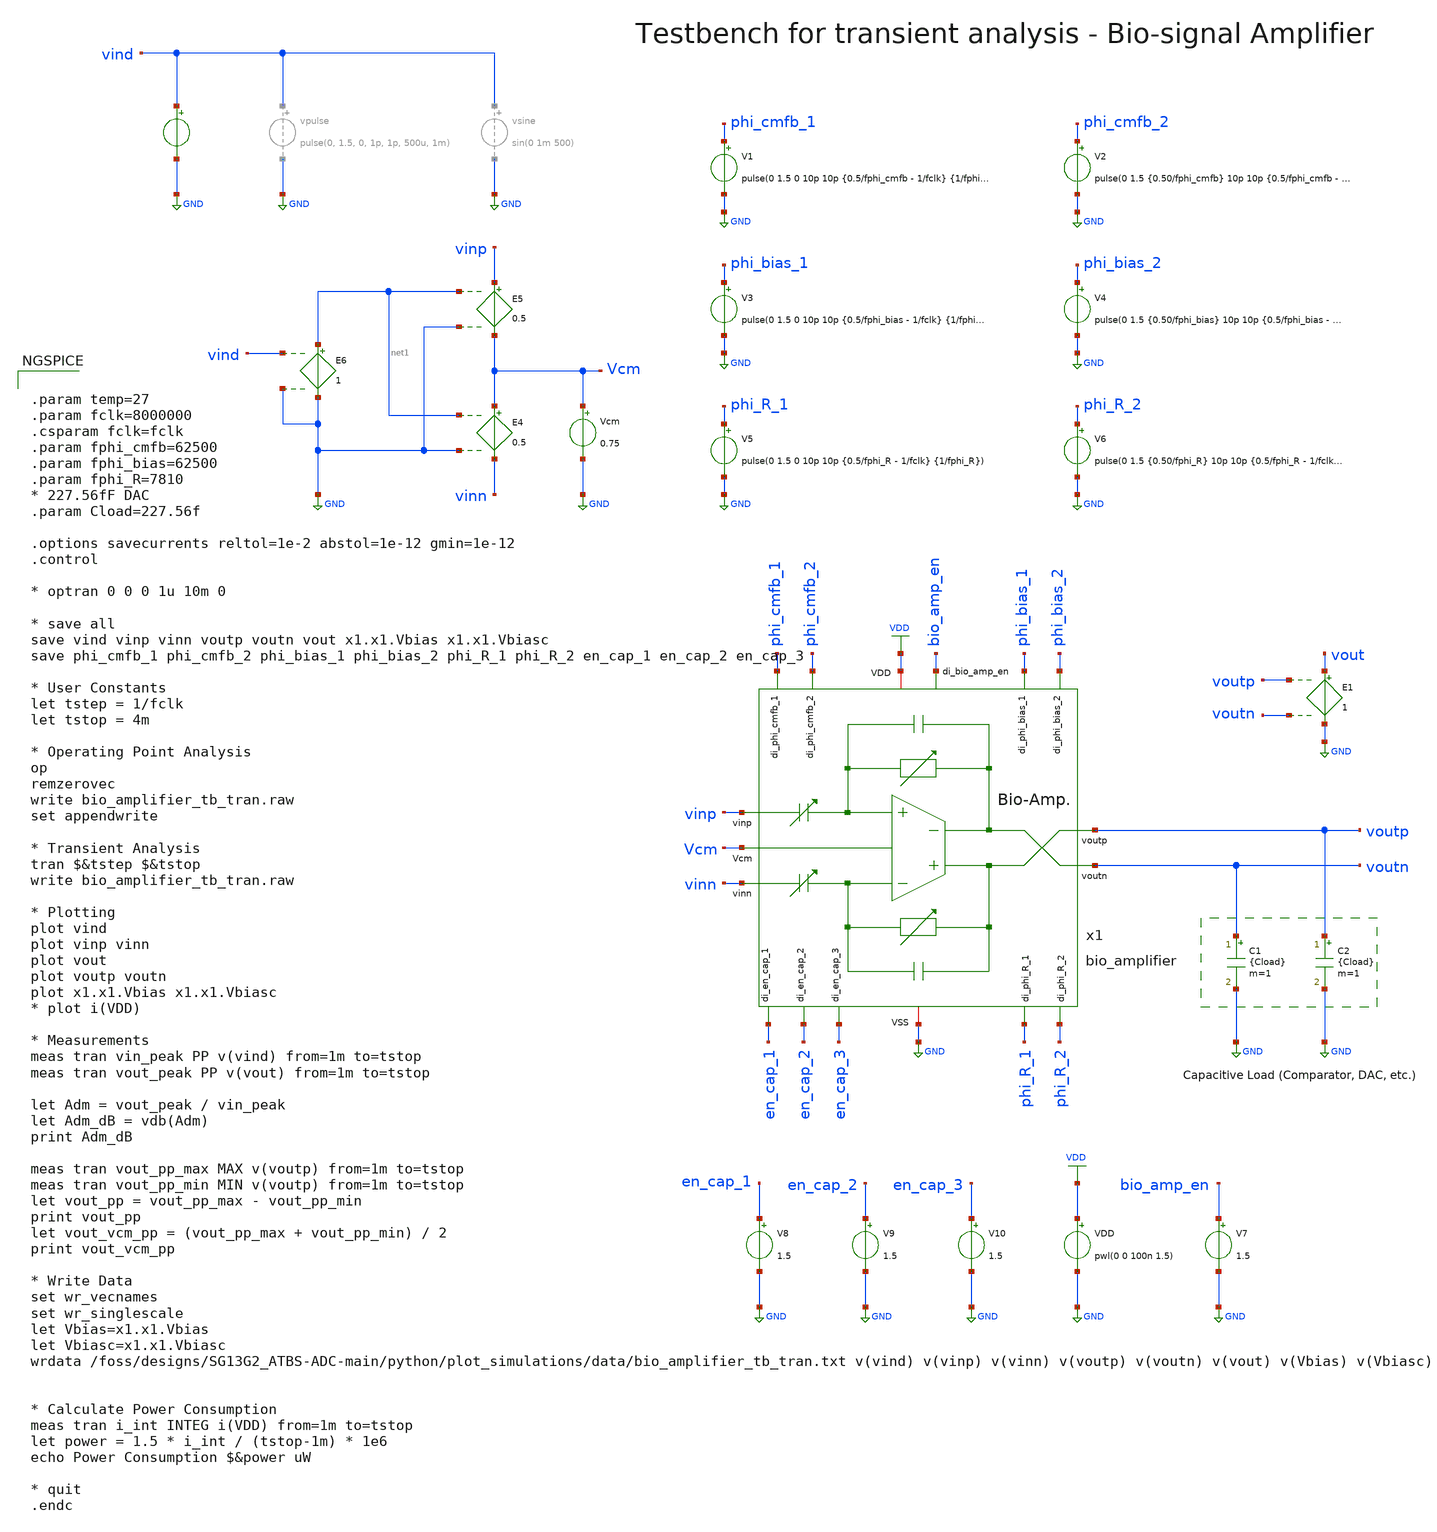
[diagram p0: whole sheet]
** sch_path: SG13G2_ATBS-ADC-main/xschem/bio_amplifier/testbenches/bio_amplifier_tb_tran.sch
**.subckt bio_amplifier_tb_tran
C1 voutn GND {Cload} m=1
x1 phi_bias_2 phi_bias_1 phi_R_2 phi_R_1 en_cap_3 en_cap_1 en_cap_2 phi_cmfb_2 phi_cmfb_1 voutp
+ bio_amp_en vinp Vcm voutn vinn VDD GND bio_amplifier
C2 voutp GND {Cload} m=1
V1 phi_cmfb_1 GND pulse(0 1.5 0 10p 10p {0.5/fphi_cmfb - 1/fclk} {1/fphi_cmfb})
Vcm Vcm GND 0.75
E4 Vcm vinn net1 GND 0.5
E5 vinp Vcm net1 GND 0.5
E6 net1 GND vind GND 1
V2 phi_cmfb_2 GND pulse(0 1.5 {0.50/fphi_cmfb} 10p 10p {0.5/fphi_cmfb - 1/fclk} {1/fphi_cmfb})
V3 phi_bias_1 GND pulse(0 1.5 0 10p 10p {0.5/fphi_bias - 1/fclk} {1/fphi_bias})
V4 phi_bias_2 GND pulse(0 1.5 {0.50/fphi_bias} 10p 10p {0.5/fphi_bias - 1/fclk} {1/fphi_bias})
V5 phi_R_1 GND pulse(0 1.5 0 10p 10p {0.5/fphi_R - 1/fclk} {1/fphi_R})
V6 phi_R_2 GND pulse(0 1.5 {0.50/fphi_R} 10p 10p {0.5/fphi_R - 1/fclk} {1/fphi_R})
V7 bio_amp_en GND 1.5
V8 en_cap_1 GND 1.5
V9 en_cap_2 GND 1.5
V10 en_cap_3 GND 1.5
VDD VDD GND pwl(0 0 100n 1.5)
E1 vout GND voutp voutn 1
vecg vind GND dc 0 pwl(0.0 -0.000131 0.0009775171065493646 -0.000108 0.0019550342130987292 -0.000111
+ 0.002932551319648094 -6.4e-05 0.0039100684261974585 -1.3e-05 0.004887585532746823 2.3e-05 0.005865102639296188 6.1e-05
+ 0.006842619745845552 7.4e-05 0.007820136852394917 3.9e-05 0.00879765395894428 3e-06 0.009775171065493646 -8e-06
+ 0.010752688172043012 6e-06 0.011730205278592375 6.9e-05 0.012707722385141739 0.000126 0.013685239491691105 0.000153
+ 0.01466275659824047 0.000114 0.015640273704789834 5.8e-05 0.016617790811339198 1e-05 0.01759530791788856 2.3e-05
+ 0.01857282502443793 5e-05 0.019550342130987292 0.000105 0.020527859237536656 0.000149 0.021505376344086023 0.000131
+ 0.022482893450635387 0.000131 0.02346041055718475 0.000132 0.024437927663734114 0.000168 0.025415444770283478 0.000199
+ 0.026392961876832845 0.000188 0.02737047898338221 0.000119 0.028347996089931573 9e-05 0.02932551319648094 8.8e-05
+ 0.030303030303030304 0.000151 0.03128054740957967 0.000221 0.03225806451612903 0.000271 0.033235581622678395 0.000312
+ 0.03421309872922776 0.000283 0.03519061583577712 0.00024 0.03616813294232649 0.00019 0.03714565004887586 0.000168
+ 0.03812316715542522 0.000166 0.039100684261974585 0.000218 0.04007820136852395 0.000249 0.04105571847507331 0.000247
+ 0.042033235581622676 0.000262 0.043010752688172046 0.000289 0.04398826979472141 0.00034 0.044965786901270774 0.000358
+ 0.04594330400782014 0.000352 0.0469208211143695 0.000299 0.047898338220918865 0.000247 0.04887585532746823 0.000226
+ 0.04985337243401759 0.000266 0.050830889540566956 0.000336 0.05180840664711633 0.000419 0.05278592375366569 0.000444
+ 0.053763440860215055 0.000379 0.05474095796676442 0.000353 0.05571847507331378 0.000351 0.056695992179863146 0.000334
+ 0.05767350928641251 0.000372 0.05865102639296188 0.000423 0.059628543499511244 0.000442 0.06060606060606061 0.000429
+ 0.06158357771260997 0.000417 0.06256109481915934 0.000427 0.0635386119257087 0.00044 0.06451612903225806 0.000458
+ 0.06549364613880743 0.000491 0.06647116324535679 0.000463 0.06744868035190615 0.000427 0.06842619745845552 0.000358
+ 0.06940371456500488 0.000386 0.07038123167155425 0.000503 0.07135874877810362 0.000571 0.07233626588465299 0.000571
+ 0.07331378299120235 0.000508 0.07429130009775171 0.000463 0.07526881720430108 0.000397 0.07624633431085044 0.000405
+ 0.0772238514173998 0.000456 0.07820136852394917 0.00046 0.07917888563049853 0.000421 0.0801564027370479 0.000345
+ 0.08113391984359726 0.000299 0.08211143695014662 0.000284 0.08308895405669599 0.000285 0.08406647116324535 0.000272
+ 0.08504398826979472 0.000269 0.08602150537634409 0.000216 0.08699902248289346 0.000144 0.08797653958944282 0.000106
+ 0.08895405669599218 0.000194 0.08993157380254155 0.00029 0.09090909090909091 0.000323 0.09188660801564028 0.000276
+ 0.09286412512218964 0.000227 0.093841642228739 0.000182 0.09481915933528837 0.000174 0.09579667644183773 0.000206
+ 0.0967741935483871 0.000235 0.09775171065493646 0.000326 0.09872922776148582 0.000412 0.09970674486803519 0.000423
+ 0.10068426197458455 0.000439 0.10166177908113391 0.000475 0.10263929618768329 0.000516 0.10361681329423265 0.000534
+ 0.10459433040078202 0.000499 0.10557184750733138 0.000411 0.10654936461388075 0.000347 0.10752688172043011 0.000343
+ 0.10850439882697947 0.000445 0.10948191593352884 0.000583 0.1104594330400782 0.000643 0.11143695014662756 0.000628
+ 0.11241446725317693 0.000517 0.11339198435972629 0.000428 0.11436950146627566 0.000371 0.11534701857282502 0.000372
+ 0.11632453567937438 0.000397 0.11730205278592376 0.000444 0.11827956989247312 0.000463 0.11925708699902249 0.000408
+ 0.12023460410557185 0.000357 0.12121212121212122 0.000329 0.12218963831867058 0.000336 0.12316715542521994 0.000336
+ 0.1241446725317693 0.000358 0.12512218963831867 0.00034 0.12609970674486803 0.000245 0.1270772238514174 0.000127
+ 0.12805474095796676 0.000156 0.12903225806451613 0.000314 0.1300097751710655 0.000435 0.13098729227761485 0.000453
+ 0.13196480938416422 0.000388 0.13294232649071358 0.00028 0.13391984359726294 0.00019 0.1348973607038123 0.000136
+ 0.13587487781036167 0.000118 0.13685239491691104 0.000121 0.1378299120234604 0.000103 0.13880742913000976 3.2e-05
+ 0.13978494623655913 -8e-06 0.1407624633431085 -1e-06 0.14173998044965788 6.8e-05 0.14271749755620725 0.00013
+ 0.1436950146627566 0.000148 0.14467253176930597 0.000105 0.14565004887585534 3.8e-05 0.1466275659824047 -1.2e-05
+ 0.14760508308895406 3.7e-05 0.14858260019550343 0.000134 0.1495601173020528 0.000186 0.15053763440860216 0.000184
+ 0.15151515151515152 0.000129 0.15249266862170088 9.4e-05 0.15347018572825025 0.00011 0.1544477028347996 0.000148
+ 0.15542521994134897 0.000212 0.15640273704789834 0.000267 0.1573802541544477 0.000262 0.15835777126099707 0.000278
+ 0.15933528836754643 0.0003 0.1603128054740958 0.00032 0.16129032258064516 0.000374 0.16226783968719452 0.000399
+ 0.16324535679374388 0.000379 0.16422287390029325 0.000301 0.1652003910068426 0.000216 0.16617790811339198 0.000145
+ 0.16715542521994134 0.000147 0.1681329423264907 0.000201 0.16911045943304007 0.000283 0.17008797653958943 0.000314
+ 0.1710654936461388 0.000282 0.17204301075268819 0.000257 0.17302052785923755 0.000186 0.1739980449657869 0.000112
+ 0.17497556207233628 7.8e-05 0.17595307917888564 8.3e-05 0.176930596285435 0.000109 0.17790811339198437 0.000138
+ 0.17888563049853373 0.000168 0.1798631476050831 0.000221 0.18084066471163246 0.000321 0.18181818181818182 0.000375
+ 0.1827956989247312 0.000353 0.18377321603128055 0.000305 0.18475073313782991 0.000222 0.18572825024437928 0.00014
+ 0.18670576735092864 0.000182 0.187683284457478 0.000301 0.18866080156402737 0.000385 0.18963831867057673 0.00039
+ 0.1906158357771261 0.000371 0.19159335288367546 0.000349 0.19257086999022482 0.000278 0.1935483870967742 0.000229
+ 0.19452590420332355 0.000235 0.19550342130987292 0.000308 0.19648093841642228 0.000349 0.19745845552297164 0.000331
+ 0.198435972629521 0.000306 0.19941348973607037 0.000272 0.20039100684261973 0.000224 0.2013685239491691 0.000192
+ 0.20234604105571846 0.00014 0.20332355816226783 8.3e-05 0.20430107526881722 5.3e-05 0.20527859237536658 7.3e-05
+ 0.20625610948191594 0.000157 0.2072336265884653 0.000239 0.20821114369501467 0.000249 0.20918866080156404 0.00018
+ 0.2101661779081134 0.000123 0.21114369501466276 0.000108 0.21212121212121213 0.000115 0.2130987292277615 0.000152
+ 0.21407624633431085 0.00017 0.21505376344086022 0.000195 0.21603128054740958 0.000218 0.21700879765395895 0.000184
+ 0.2179863147605083 0.000142 0.21896383186705767 0.000148 0.21994134897360704 0.000226 0.2209188660801564 0.000283
+ 0.22189638318670576 0.000253 0.22287390029325513 0.000162 0.2238514173998045 4.2e-05 0.22482893450635386 -5.4e-05
+ 0.22580645161290322 -1.1e-05 0.22678396871945258 0.000119 0.22776148582600195 0.000213 0.2287390029325513 0.000279
+ 0.22971652003910067 0.000278 0.23069403714565004 0.000254 0.2316715542521994 0.000201 0.23264907135874877 0.000145
+ 0.23362658846529813 0.000119 0.23460410557184752 0.00013 0.23558162267839688 0.000149 0.23655913978494625 0.000125
+ 0.2375366568914956 0.000126 0.23851417399804498 0.000164 0.23949169110459434 0.000229 0.2404692082111437 0.000271
+ 0.24144672531769307 0.000288 0.24242424242424243 0.000261 0.2434017595307918 0.000226 0.24437927663734116 0.000183
+ 0.24535679374389052 0.000244 0.24633431085043989 0.000347 0.24731182795698925 0.000349 0.2482893450635386 0.000275
+ 0.24926686217008798 0.000182 0.25024437927663734 0.000139 0.2512218963831867 9.6e-05 0.25219941348973607 0.000125
+ 0.25317693059628543 0.000179 0.2541544477028348 0.000249 0.25513196480938416 0.000299 0.2561094819159335 0.000279
+ 0.2570869990224829 0.000229 0.25806451612903225 0.00017 0.2590420332355816 0.000103 0.260019550342131 8.8e-05
+ 0.26099706744868034 0.000129 0.2619745845552297 0.000111 0.26295210166177907 8.6e-05 0.26392961876832843 4.5e-05
+ 0.2649071358748778 9.2e-05 0.26588465298142716 0.000159 0.2668621700879765 0.000149 0.2678396871945259 0.000107
+ 0.26881720430107525 7.1e-05 0.2697947214076246 6.6e-05 0.270772238514174 9.7e-05 0.27174975562072334 0.000142
+ 0.2727272727272727 0.000138 0.27370478983382207 0.000146 0.27468230694037143 0.000155 0.2756598240469208 0.000134
+ 0.27663734115347016 0.000114 0.2776148582600195 0.000107 0.2785923753665689 0.000118 0.27956989247311825 0.000107
+ 0.2805474095796676 0.000131 0.281524926686217 0.000142 0.2825024437927664 8.4e-05 0.28347996089931576 2.5e-05
+ 0.2844574780058651 4.4e-05 0.2854349951124145 0.000113 0.28641251221896386 0.000182 0.2873900293255132 0.000234
+ 0.2883675464320626 0.000205 0.28934506353861195 0.000135 0.2903225806451613 3.7e-05 0.2913000977517107 1e-05
+ 0.29227761485826004 3e-05 0.2932551319648094 7.5e-05 0.29423264907135877 0.000132 0.29521016617790813 0.000127
+ 0.2961876832844575 0.000113 0.29716520039100686 0.000127 0.2981427174975562 0.000158 0.2991202346041056 0.000169
+ 0.30009775171065495 0.000173 0.3010752688172043 0.000123 0.3020527859237537 7.9e-05 0.30303030303030304 6.9e-05
+ 0.3040078201368524 0.000119 0.30498533724340177 0.00017 0.30596285434995113 0.000179 0.3069403714565005 0.000204
+ 0.30791788856304986 0.000183 0.3088954056695992 0.000138 0.3098729227761486 0.000119 0.31085043988269795 0.000169
+ 0.3118279569892473 0.000212 0.3128054740957967 0.000228 0.31378299120234604 0.000223 0.3147605083088954 0.000176
+ 0.31573802541544477 0.000181 0.31671554252199413 0.000235 0.3176930596285435 0.000327 0.31867057673509286 0.000415
+ 0.3196480938416422 0.000428 0.3206256109481916 0.000366 0.32160312805474095 0.00031 0.3225806451612903 0.0003
+ 0.3235581622678397 0.000374 0.32453567937438904 0.000488 0.3255131964809384 0.000562 0.32649071358748777 0.000571
+ 0.32746823069403713 0.000514 0.3284457478005865 0.000488 0.32942326490713586 0.000492 0.3304007820136852 0.000505
+ 0.3313782991202346 0.000507 0.33235581622678395 0.000521 0.3333333333333333 0.000499 0.3343108504398827 0.000445
+ 0.33528836754643204 0.000408 0.3362658846529814 0.000399 0.33724340175953077 0.000435 0.33822091886608013 0.000452
+ 0.3391984359726295 0.000437 0.34017595307917886 0.000367 0.3411534701857282 0.000282 0.3421309872922776 0.000234
+ 0.34310850439882695 0.000305 0.34408602150537637 0.000396 0.34506353861192574 0.00042 0.3460410557184751 0.000399
+ 0.34701857282502446 0.000327 0.3479960899315738 0.000273 0.3489736070381232 0.000247 0.34995112414467255 0.000229
+ 0.3509286412512219 0.000237 0.3519061583577713 0.000284 0.35288367546432065 0.000299 0.35386119257087 0.000267
+ 0.3548387096774194 0.000216 0.35581622678396874 0.00019 0.3567937438905181 0.000197 0.35777126099706746 0.000198
+ 0.3587487781036168 0.000144 0.3597262952101662 4.4e-05 0.36070381231671556 -0.000126 0.3616813294232649 -0.00024
+ 0.3626588465298143 -0.000223 0.36363636363636365 -0.000153 0.364613880742913 -0.000106 0.3655913978494624 -8.6e-05
+ 0.36656891495601174 -0.000102 0.3675464320625611 -0.000158 0.36852394916911047 -0.000205 0.36950146627565983 -0.000204
+ 0.3704789833822092 -0.000178 0.37145650048875856 -0.000119 0.3724340175953079 -5.3e-05 0.3734115347018573 -5e-05
+ 0.37438905180840665 -8e-06 0.375366568914956 4.9e-05 0.3763440860215054 0.000102 0.37732160312805474 0.000105
+ 0.3782991202346041 9.7e-05 0.37927663734115347 6.9e-05 0.38025415444770283 3.2e-05 0.3812316715542522 3e-06
+ 0.38220918866080156 5e-05 0.3831867057673509 0.000153 0.3841642228739003 0.000231 0.38514173998044965 0.000253
+ 0.386119257086999 0.000215 0.3870967741935484 0.000146 0.38807429130009774 9.5e-05 0.3890518084066471 8.6e-05
+ 0.39002932551319647 0.000112 0.39100684261974583 0.000142 0.3919843597262952 0.000126 0.39296187683284456 5.6e-05
+ 0.3939393939393939 1.8e-05 0.3949169110459433 5e-06 0.39589442815249265 2.7e-05 0.396871945259042 4.9e-05
+ 0.3978494623655914 5.5e-05 0.39882697947214074 9e-06 0.3998044965786901 -7.3e-05 0.40078201368523947 -0.00013
+ 0.40175953079178883 -6e-05 0.4027370478983382 5.5e-05 0.40371456500488756 0.000123 0.4046920821114369 9.7e-05
+ 0.4056695992179863 6e-06 0.40664711632453565 -6.2e-05 0.40762463343108507 -0.000114 0.40860215053763443 -0.000136
+ 0.4095796676441838 -0.000125 0.41055718475073316 -7.8e-05 0.4115347018572825 -3.9e-05 0.4125122189638319 -6.7e-05
+ 0.41348973607038125 -7.1e-05 0.4144672531769306 -6.9e-05 0.41544477028348 -2.1e-05 0.41642228739002934 2.7e-05
+ 0.4173998044965787 3.6e-05 0.41837732160312807 -1.1e-05 0.41935483870967744 -0.000105 0.4203323558162268 -0.000175
+ 0.42130987292277616 -0.000141 0.4222873900293255 -2.7e-05 0.4232649071358749 5e-06 0.42424242424242425 1.4e-05
+ 0.4252199413489736 -3.7e-05 0.426197458455523 -9.8e-05 0.42717497556207235 -0.000144 0.4281524926686217 -0.000166
+ 0.4291300097751711 -0.000177 0.43010752688172044 -0.000154 0.4310850439882698 -0.000131 0.43206256109481916 -0.000154
+ 0.43304007820136853 -0.000186 0.4340175953079179 -0.000208 0.43499511241446726 -0.000175 0.4359726295210166 -0.000155
+ 0.436950146627566 -0.000131 0.43792766373411535 -0.00012 0.4389051808406647 -0.000163 0.4398826979472141 -0.000226
+ 0.44086021505376344 -0.000195 0.4418377321603128 -0.000106 0.44281524926686217 -6e-05 0.44379276637341153 -5.9e-05
+ 0.4447702834799609 -9.6e-05 0.44574780058651026 -0.000166 0.4467253176930596 -0.000199 0.447702834799609 -0.000176
+ 0.44868035190615835 -0.0001 0.4496578690127077 -4.7e-05 0.4506353861192571 -1.7e-05 0.45161290322580644 -6e-06
+ 0.4525904203323558 -1.8e-05 0.45356793743890517 -6e-06 0.45454545454545453 4.9e-05 0.4555229716520039 0.000102
+ 0.45650048875855326 0.000135 0.4574780058651026 0.000124 0.458455522971652 5.1e-05 0.45943304007820135 -1.9e-05
+ 0.4604105571847507 3.4e-05 0.4613880742913001 0.000116 0.46236559139784944 0.000158 0.4633431085043988 0.000175
+ 0.46432062561094817 0.000136 0.46529814271749753 0.000119 0.4662756598240469 0.00011 0.46725317693059626 0.000113
+ 0.4682306940371456 0.000145 0.46920821114369504 0.000136 0.4701857282502444 8.4e-05 0.47116324535679377 1.6e-05
+ 0.47214076246334313 -2.1e-05 0.4731182795698925 -1.9e-05 0.47409579667644186 6e-06 0.4750733137829912 4.7e-05
+ 0.4760508308895406 5.6e-05 0.47702834799608995 3e-06 0.4780058651026393 -7.5e-05 0.4789833822091887 -0.00016
+ 0.47996089931573804 -0.000129 0.4809384164222874 -1.7e-05 0.48191593352883677 3.1e-05 0.48289345063538613 -2.8e-05
+ 0.4838709677419355 -0.000118 0.48484848484848486 -0.000184 0.4858260019550342 -0.000233 0.4868035190615836 -0.00021
+ 0.48778103616813295 -0.000166 0.4887585532746823 -0.000112 0.4897360703812317 -0.00011 0.49071358748778104 -0.000163
+ 0.4916911045943304 -0.000263 0.49266862170087977 -0.000345 0.49364613880742914 -0.00034 0.4946236559139785 -0.000303
+ 0.49560117302052786 -0.000282 0.4965786901270772 -0.00028 0.4975562072336266 -0.000269 0.49853372434017595 -0.000242
+ 0.4995112414467253 -0.000114 0.5004887585532747 8.1e-05 0.501466275659824 0.000227 0.5024437927663734 0.000365
+ 0.5034213098729228 0.00049 0.5043988269794721 0.000669 0.5053763440860215 0.000888 0.5063538611925709 0.001169
+ 0.5073313782991202 0.001511 0.5083088954056696 0.001889 0.509286412512219 0.002282 0.5102639296187683 0.002675
+ 0.5112414467253177 0.0031 0.512218963831867 0.003523 0.5131964809384164 0.003975 0.5141739980449658 0.004458
+ 0.5151515151515151 0.004932 0.5161290322580645 0.005347 0.5171065493646139 0.005737 0.5180840664711632 0.005689
+ 0.5190615835777126 0.005641 0.520039100684262 0.005592 0.5210166177908113 0.005544 0.5219941348973607 0.005499
+ 0.52297165200391 0.00546 0.5239491691104594 0.005402 0.5249266862170088 0.005351 0.5259042033235581 0.005305
+ 0.5268817204301075 0.005256 0.5278592375366569 0.005208 0.5288367546432062 0.005162 0.5298142717497556 0.005114
+ 0.530791788856305 0.005067 0.5317693059628543 0.005014 0.5327468230694037 0.004876 0.533724340175953 0.004317
+ 0.5347018572825024 0.003586 0.5356793743890518 0.002638 0.5366568914956011 0.0016 0.5376344086021505 0.000579
+ 0.5386119257086999 -0.000384 0.5395894428152492 -0.001299 0.5405669599217986 -0.00209 0.541544477028348 -0.002742
+ 0.5425219941348973 -0.003288 0.5434995112414467 -0.003693 0.544477028347996 -0.00395 0.5454545454545454 -0.004134
+ 0.5464320625610948 -0.004263 0.5474095796676441 -0.004256 0.5483870967741935 -0.004161 0.5493646138807429 -0.004005
+ 0.5503421309872922 -0.003771 0.5513196480938416 -0.003495 0.552297165200391 -0.003203 0.5532746823069403 -0.002886
+ 0.5542521994134897 -0.002636 0.555229716520039 -0.002487 0.5562072336265884 -0.002389 0.5571847507331378 -0.002295
+ 0.5581622678396871 -0.002116 0.5591397849462365 -0.001913 0.5601173020527859 -0.001772 0.5610948191593352 -0.001703
+ 0.5620723362658846 -0.001719 0.563049853372434 -0.001754 0.5640273704789834 -0.001799 0.5650048875855328 -0.001765
+ 0.5659824046920822 -0.001724 0.5669599217986315 -0.001667 0.5679374389051809 -0.001621 0.5689149560117303 -0.001606
+ 0.5698924731182796 -0.001587 0.570869990224829 -0.001518 0.5718475073313783 -0.0014 0.5728250244379277 -0.001321
+ 0.5738025415444771 -0.001276 0.5747800586510264 -0.00127 0.5757575757575758 -0.001281 0.5767350928641252 -0.001261
+ 0.5777126099706745 -0.001168 0.5786901270772239 -0.001068 0.5796676441837733 -0.001038 0.5806451612903226 -0.001059
+ 0.581622678396872 -0.001108 0.5826001955034213 -0.001203 0.5835777126099707 -0.001281 0.5845552297165201 -0.001334
+ 0.5855327468230694 -0.001326 0.5865102639296188 -0.001254 0.5874877810361682 -0.001227 0.5884652981427175 -0.001256
+ 0.5894428152492669 -0.001247 0.5904203323558163 -0.001218 0.5913978494623656 -0.001144 0.592375366568915 -0.001087
+ 0.5933528836754643 -0.001075 0.5943304007820137 -0.00112 0.5953079178885631 -0.001185 0.5962854349951124 -0.00119
+ 0.5972629521016618 -0.001113 0.5982404692082112 -0.001016 0.5992179863147605 -0.000966 0.6001955034213099 -0.00093
+ 0.6011730205278593 -0.000947 0.6021505376344086 -0.000956 0.603128054740958 -0.000958 0.6041055718475073 -0.000928
+ 0.6050830889540567 -0.000851 0.6060606060606061 -0.000792 0.6070381231671554 -0.000744 0.6080156402737048 -0.000758
+ 0.6089931573802542 -0.000775 0.6099706744868035 -0.000758 0.6109481915933529 -0.000695 0.6119257086999023 -0.000584
+ 0.6129032258064516 -0.000557 0.613880742913001 -0.000599 0.6148582600195504 -0.000667 0.6158357771260997 -0.000701
+ 0.6168132942326491 -0.000638 0.6177908113391984 -0.000526 0.6187683284457478 -0.000457 0.6197458455522972 -0.0004
+ 0.6207233626588465 -0.000407 0.6217008797653959 -0.000427 0.6226783968719453 -0.000475 0.6236559139784946 -0.00049
+ 0.624633431085044 -0.000498 0.6256109481915934 -0.000488 0.6265884652981427 -0.000499 0.6275659824046921 -0.000514
+ 0.6285434995112414 -0.000555 0.6295210166177908 -0.000537 0.6304985337243402 -0.000427 0.6314760508308895 -0.000359
+ 0.6324535679374389 -0.00033 0.6334310850439883 -0.000366 0.6344086021505376 -0.000428 0.635386119257087 -0.000484
+ 0.6363636363636364 -0.000426 0.6373411534701857 -0.000321 0.6383186705767351 -0.000229 0.6392961876832844 -0.000201
+ 0.6402737047898338 -0.000206 0.6412512218963832 -0.00024 0.6422287390029325 -0.000269 0.6432062561094819 -0.000253
+ 0.6441837732160313 -0.000214 0.6451612903225806 -0.000173 0.64613880742913 -0.000168 0.6471163245356794 -0.000208
+ 0.6480938416422287 -0.000204 0.6490713587487781 -0.000155 0.6500488758553274 -0.0001 0.6510263929618768 -9.4e-05
+ 0.6520039100684262 -0.000143 0.6529814271749755 -0.000186 0.6539589442815249 -0.000187 0.6549364613880743 -0.000179
+ 0.6559139784946236 -0.000149 0.656891495601173 -8.2e-05 0.6578690127077224 -4.1e-05 0.6588465298142717 -7.6e-05
+ 0.6598240469208211 -0.000109 0.6608015640273704 -9.9e-05 0.6617790811339198 -0.000111 0.6627565982404692 -0.000128
+ 0.6637341153470185 -0.000122 0.6647116324535679 -7.6e-05 0.6656891495601173 -6.2e-05 0.6666666666666666 -5e-05
+ 0.667644183773216 -2.1e-05 0.6686217008797654 8e-06 0.6695992179863147 4.4e-05 0.6705767350928641 9.4e-05
+ 0.6715542521994134 0.000124 0.6725317693059628 5.5e-05 0.6735092864125122 -3.2e-05 0.6744868035190615 -8.2e-05
+ 0.6754643206256109 7e-06 0.6764418377321603 0.000132 0.6774193548387096 0.000184 0.678396871945259 0.000148
+ 0.6793743890518084 6.2e-05 0.6803519061583577 -5.8e-05 0.6813294232649071 -0.00014 0.6823069403714564 -0.00014
+ 0.6832844574780058 -0.000101 0.6842619745845552 -0.000101 0.6852394916911045 -0.000138 0.6862170087976539 -0.000212
+ 0.6871945259042033 -0.000262 0.6881720430107527 -0.000242 0.6891495601173021 -0.000169 0.6901270772238515 -9.5e-05
+ 0.6911045943304008 -5.6e-05 0.6920821114369502 -8.6e-05 0.6930596285434996 -0.000174 0.6940371456500489 -0.000221
+ 0.6950146627565983 -0.000147 0.6959921798631477 -3.8e-05 0.696969696969697 4.4e-05 0.6979472140762464 0.000112
+ 0.6989247311827957 0.000103 0.6999022482893451 0.000103 0.7008797653958945 7.9e-05 0.7018572825024438 0.000104
+ 0.7028347996089932 0.000153 0.7038123167155426 0.000203 0.7047898338220919 0.000218 0.7057673509286413 0.000183
+ 0.7067448680351907 0.000188 0.70772238514174 0.000234 0.7086999022482894 0.000286 0.7096774193548387 0.000319
+ 0.7106549364613881 0.000338 0.7116324535679375 0.000286 0.7126099706744868 0.000233 0.7135874877810362 0.000194
+ 0.7145650048875856 0.000228 0.7155425219941349 0.000305 0.7165200391006843 0.000316 0.7174975562072337 0.000275
+ 0.718475073313783 0.000219 0.7194525904203324 0.000177 0.7204301075268817 0.000149 0.7214076246334311 0.000159
+ 0.7223851417399805 0.00021 0.7233626588465298 0.000332 0.7243401759530792 0.000431 0.7253176930596286 0.000418
+ 0.7262952101661779 0.000423 0.7272727272727273 0.00044 0.7282502443792767 0.000442 0.729227761485826 0.000438
+ 0.7302052785923754 0.000414 0.7311827956989247 0.000335 0.7321603128054741 0.000264 0.7331378299120235 0.000259
+ 0.7341153470185728 0.000338 0.7350928641251222 0.00045 0.7360703812316716 0.00051 0.7370478983382209 0.000519
+ 0.7380254154447703 0.000481 0.7390029325513197 0.000454 0.739980449657869 0.000462 0.7409579667644184 0.000458
+ 0.7419354838709677 0.00044 0.7429130009775171 0.000451 0.7438905180840665 0.000435 0.7448680351906158 0.000377
+ 0.7458455522971652 0.000363 0.7468230694037146 0.000375 0.7478005865102639 0.00043 0.7487781036168133 0.000478
+ 0.7497556207233627 0.000468 0.750733137829912 0.00042 0.7517106549364614 0.000361 0.7526881720430108 0.000363
+ 0.7536656891495601 0.00048 0.7546432062561095 0.000586 0.7556207233626588 0.000664 0.7565982404692082 0.000695
+ 0.7575757575757576 0.000681 0.7585532746823069 0.000697 0.7595307917888563 0.000766 0.7605083088954057 0.000852
+ 0.761485826001955 0.000911 0.7624633431085044 0.00101 0.7634408602150538 0.001051 0.7644183773216031 0.001029
+ 0.7653958944281525 0.001017 0.7663734115347018 0.00101 0.7673509286412512 0.001045 0.7683284457478006 0.001074
+ 0.7693059628543499 0.001109 0.7702834799608993 0.001113 0.7712609970674487 0.001098 0.772238514173998 0.001095
+ 0.7732160312805474 0.001158 0.7741935483870968 0.001206 0.7751710654936461 0.001227 0.7761485826001955 0.001221
+ 0.7771260997067448 0.001196 0.7781036168132942 0.001168 0.7790811339198436 0.001172 0.7800586510263929 0.001207
+ 0.7810361681329423 0.001273 0.7820136852394917 0.001349 0.782991202346041 0.001394 0.7839687194525904 0.001409
+ 0.7849462365591398 0.001451 0.7859237536656891 0.001486 0.7869012707722385 0.001549 0.7878787878787878 0.001631
+ 0.7888563049853372 0.00168 0.7898338220918866 0.001704 0.7908113391984359 0.001721 0.7917888563049853 0.001733
+ 0.7927663734115347 0.001814 0.793743890518084 0.001929 0.7947214076246334 0.001997 0.7956989247311828 0.002036
+ 0.7966764418377321 0.002051 0.7976539589442815 0.002076 0.7986314760508308 0.002057 0.7996089931573802 0.002031
+ 0.8005865102639296 0.002011 0.8015640273704789 0.001979 0.8025415444770283 0.001927 0.8035190615835777 0.001898
+ 0.804496578690127 0.00194 0.8054740957966764 0.001984 0.8064516129032258 0.002021 0.8074291300097751 0.002049
+ 0.8084066471163245 0.002042 0.8093841642228738 0.001981 0.8103616813294232 0.001913 0.8113391984359726 0.001853
+ 0.8123167155425219 0.001866 0.8132942326490713 0.001935 0.8142717497556208 0.001979 0.8152492668621701 0.001944
+ 0.8162267839687195 0.001838 0.8172043010752689 0.001777 0.8181818181818182 0.00174 0.8191593352883676 0.001708
+ 0.820136852394917 0.001757 0.8211143695014663 0.001821 0.8220918866080157 0.001892 0.823069403714565 0.001879
+ 0.8240469208211144 0.001789 0.8250244379276638 0.001696 0.8260019550342131 0.001681 0.8269794721407625 0.00169
+ 0.8279569892473119 0.001661 0.8289345063538612 0.001577 0.8299120234604106 0.001465 0.83088954056696 0.001365
+ 0.8318670576735093 0.001369 0.8328445747800587 0.001411 0.833822091886608 0.001432 0.8347996089931574 0.001358
+ 0.8357771260997068 0.001227 0.8367546432062561 0.001154 0.8377321603128055 0.001094 0.8387096774193549 0.001048
+ 0.8396871945259042 0.000988 0.8406647116324536 0.000962 0.841642228739003 0.000871 0.8426197458455523 0.000704
+ 0.8435972629521017 0.000566 0.844574780058651 0.00051 0.8455522971652004 0.000463 0.8465298142717498 0.000423
+ 0.8475073313782991 0.000329 0.8484848484848485 0.000158 0.8494623655913979 -1.7e-05 0.8504398826979472 -0.000158
+ 0.8514173998044966 -0.000203 0.852394916911046 -0.000227 0.8533724340175953 -0.000279 0.8543499511241447 -0.000349
+ 0.855327468230694 -0.000465 0.8563049853372434 -0.000588 0.8572825024437928 -0.00077 0.8582600195503421 -0.0009
+ 0.8592375366568915 -0.000995 0.8602150537634409 -0.001053 0.8611925708699902 -0.001167 0.8621700879765396 -0.001293
+ 0.863147605083089 -0.001376 0.8641251221896383 -0.00142 0.8651026392961877 -0.001398 0.8660801564027371 -0.001415
+ 0.8670576735092864 -0.001501 0.8680351906158358 -0.001623 0.8690127077223851 -0.001724 0.8699902248289345 -0.001808
+ 0.8709677419354839 -0.001818 0.8719452590420332 -0.0018 0.8729227761485826 -0.001842 0.873900293255132 -0.001916
+ 0.8748778103616813 -0.001992 0.8758553274682307 -0.002068 0.8768328445747801 -0.002182 0.8778103616813294 -0.002272
+ 0.8787878787878788 -0.002282 0.8797653958944281 -0.002273 0.8807429130009775 -0.002306 0.8817204301075269 -0.002363
+ 0.8826979472140762 -0.002425 0.8836754643206256 -0.002447 0.884652981427175 -0.002425 0.8856304985337243 -0.002402
+ 0.8866080156402737 -0.002416 0.8875855327468231 -0.002466 0.8885630498533724 -0.002547 0.8895405669599218 -0.002637
+ 0.8905180840664711 -0.002647 0.8914956011730205 -0.002587 0.8924731182795699 -0.002591 0.8934506353861192 -0.002606
+ 0.8944281524926686 -0.002619 0.895405669599218 -0.002638 0.8963831867057673 -0.002645 0.8973607038123167 -0.002602
+ 0.8983382209188661 -0.002549 0.8993157380254154 -0.002462 0.9002932551319648 -0.002389 0.9012707722385142 -0.002382
+ 0.9022482893450635 -0.002372 0.9032258064516129 -0.002373 0.9042033235581622 -0.002366 0.9051808406647116 -0.002338
+ 0.906158357771261 -0.002366 0.9071358748778103 -0.002381 0.9081133919843597 -0.002415 0.9090909090909091 -0.002487
+ 0.9100684261974584 -0.002418 0.9110459433040078 -0.002272 0.9120234604105572 -0.002206 0.9130009775171065 -0.002179
+ 0.9139784946236559 -0.002244 0.9149560117302052 -0.002305 0.9159335288367546 -0.002353 0.916911045943304 -0.002356
+ 0.9178885630498533 -0.002314 0.9188660801564027 -0.002201 0.9198435972629521 -0.002119 0.9208211143695014 -0.002123
+ 0.9217986314760508 -0.002132 0.9227761485826002 -0.002145 0.9237536656891495 -0.002115 0.9247311827956989 -0.002055
+ 0.9257086999022482 -0.002005 0.9266862170087976 -0.001975 0.927663734115347 -0.001979 0.9286412512218963 -0.001991
+ 0.9296187683284457 -0.001882 0.9305962854349951 -0.001751 0.9315738025415444 -0.00169 0.9325513196480938 -0.001704
+ 0.9335288367546432 -0.001733 0.9345063538611925 -0.001759 0.9354838709677419 -0.00174 0.9364613880742912 -0.001669
+ 0.9374389051808406 -0.001595 0.9384164222873901 -0.001531 0.9393939393939394 -0.001492 0.9403714565004888 -0.001488
+ 0.9413489736070382 -0.00146 0.9423264907135875 -0.00147 0.9433040078201369 -0.001472 0.9442815249266863 -0.001457
+ 0.9452590420332356 -0.001441 0.946236559139785 -0.00145 0.9472140762463344 -0.001453 0.9481915933528837 -0.00147
+ 0.9491691104594331 -0.001414 0.9501466275659824 -0.001336 0.9511241446725318 -0.001297 0.9521016617790812 -0.001288
+ 0.9530791788856305 -0.001277 0.9540566959921799 -0.001231 0.9550342130987293 -0.001188 0.9560117302052786 -0.001131
+ 0.956989247311828 -0.001108 0.9579667644183774 -0.001076 0.9589442815249267 -0.001042 0.9599217986314761 -0.001045
+ 0.9608993157380255 -0.001023 0.9618768328445748 -0.000975 0.9628543499511242 -0.000914 0.9638318670576735 -0.000838
+ 0.9648093841642229 -0.0008 0.9657869012707723 -0.000796 0.9667644183773216 -0.000844 0.967741935483871 -0.000879
+ 0.9687194525904204 -0.000808 0.9696969696969697 -0.000708 0.9706744868035191 -0.000665 0.9716520039100685 -0.00066
+ 0.9726295210166178 -0.000677 0.9736070381231672 -0.000658 0.9745845552297165 -0.000657 0.9755620723362659 -0.00065
+ 0.9765395894428153 -0.000647 0.9775171065493646 -0.00064 0.978494623655914 -0.000633 0.9794721407624634 -0.00064
+ 0.9804496578690127 -0.000634 0.9814271749755621 -0.000582 0.9824046920821115 -0.000498 0.9833822091886608 -0.000451
+ 0.9843597262952102 -0.000461 0.9853372434017595 -0.000515 0.9863147605083089 -0.000601 0.9872922776148583 -0.00066
+ 0.9882697947214076 -0.000611 0.989247311827957 -0.000516 0.9902248289345064 -0.000448 0.9912023460410557 -0.000465
+ 0.9921798631476051 -0.00048 0.9931573802541545 -0.000472 0.9941348973607038 -0.000448 0.9951124144672532 -0.000415
+ 0.9960899315738025 -0.000375 0.9970674486803519 -0.00031 0.9980449657869013 -0.000278 0.9990224828934506 -0.000303 1.0
+ -0.000347 )
**** begin user architecture code

.lib cornerMOSlv.lib mos_tt
.lib cornerMOShv.lib mos_tt
.lib cornerRES.lib res_typ



.param temp=27
.param fclk=8000000
.csparam fclk=fclk
.param fphi_cmfb=62500
.param fphi_bias=62500
.param fphi_R=7810
* 227.56fF DAC
.param Cload=227.56f

.options savecurrents reltol=1e-2 abstol=1e-12 gmin=1e-12
.control

* optran 0 0 0 1u 10m 0

* save all
save vind vinp vinn voutp voutn vout x1.x1.Vbias x1.x1.Vbiasc
save phi_cmfb_1 phi_cmfb_2 phi_bias_1 phi_bias_2 phi_R_1 phi_R_2 en_cap_1 en_cap_2 en_cap_3

* User Constants
let tstep = 1/fclk
let tstop = 4m

* Operating Point Analysis
op
remzerovec
write bio_amplifier_tb_tran.raw
set appendwrite

* Transient Analysis
tran $&tstep $&tstop
write bio_amplifier_tb_tran.raw

* Plotting
plot vind
plot vinp vinn
plot vout
plot voutp voutn
plot x1.x1.Vbias x1.x1.Vbiasc
* plot i(VDD)

* Measurements
meas tran vin_peak PP v(vind) from=1m to=tstop
meas tran vout_peak PP v(vout) from=1m to=tstop

let Adm = vout_peak / vin_peak
let Adm_dB = vdb(Adm)
print Adm_dB

meas tran vout_pp_max MAX v(voutp) from=1m to=tstop
meas tran vout_pp_min MIN v(voutp) from=1m to=tstop
let vout_pp = vout_pp_max - vout_pp_min
print vout_pp
let vout_vcm_pp = (vout_pp_max + vout_pp_min) / 2
print vout_vcm_pp

* Write Data
set wr_vecnames
set wr_singlescale
let Vbias=x1.x1.Vbias
let Vbiasc=x1.x1.Vbiasc
wrdata /foss/designs/SG13G2_ATBS-ADC-main/python/plot_simulations/data/bio_amplifier_tb_tran.txt
+ v(vind) v(vinp) v(vinn) v(voutp) v(voutn) v(vout) v(Vbias) v(Vbiasc)


* Calculate Power Consumption
meas tran i_int INTEG i(VDD) from=1m to=tstop
let power = 1.5 * i_int / (tstop-1m) * 1e6
echo Power Consumption $&power uW

* quit
.endc


**** end user architecture code
**.ends
.GLOBAL GND
.GLOBAL VDD
.end
